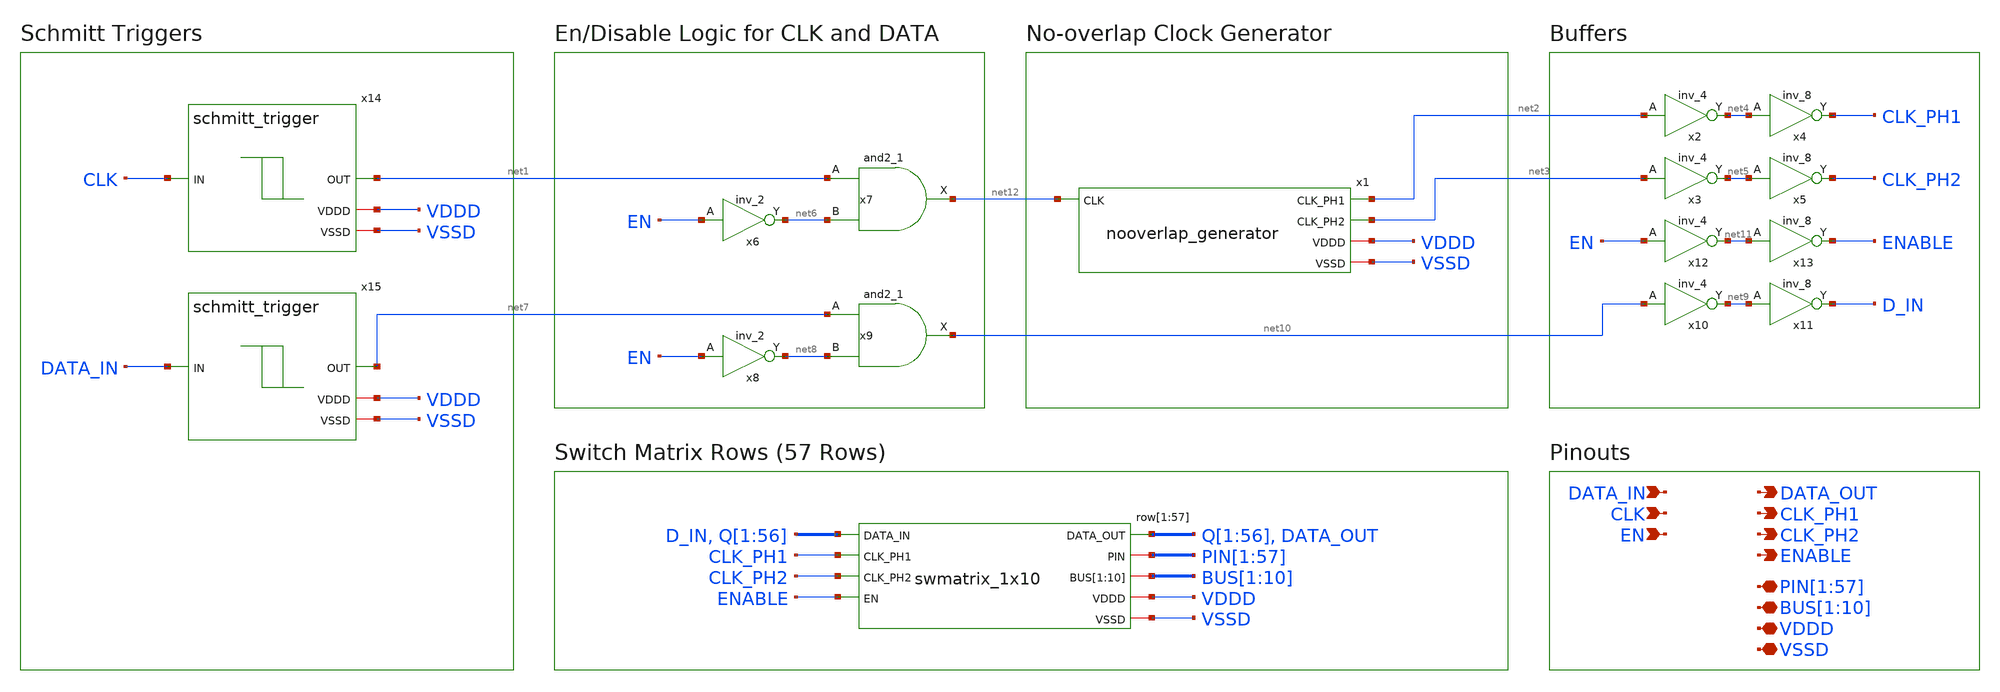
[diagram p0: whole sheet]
** sch_path: designs/libs/core_switch_matrix/swmatrix_57x10/swmatrix_57x10.sch
**.subckt swmatrix_57x10 DATA_IN CLK DATA_OUT VDDD VSSD EN
*+ PIN[1],PIN[2],PIN[3],PIN[4],PIN[5],PIN[6],PIN[7],PIN[8],PIN[9],PIN[10],PIN[11],PIN[12],PIN[13],PIN[14],PIN[15],PIN[16],PIN[17],PIN[18],PIN[19],PIN[20],PIN[21],PIN[22],PIN[23],PIN[24],PIN[25],PIN[26],PIN[27],PIN[28],PIN[29],PIN[30],PIN[31],PIN[32],PIN[33],PIN[34],PIN[35],PIN[36],PIN[37],PIN[38],PIN[39],PIN[40],PIN[41],PIN[42],PIN[43],PIN[44],PIN[45],PIN[46],PIN[47],PIN[48],PIN[49],PIN[50],PIN[51],PIN[52],PIN[53],PIN[54],PIN[55],PIN[56],PIN[57] BUS[1],BUS[2],BUS[3],BUS[4],BUS[5],BUS[6],BUS[7],BUS[8],BUS[9],BUS[10] CLK_PH1 CLK_PH2 ENABLE
*.ipin DATA_IN
*.ipin CLK
*.opin DATA_OUT
*.iopin VDDD
*.iopin VSSD
*.ipin EN
*.iopin
*+ PIN[1],PIN[2],PIN[3],PIN[4],PIN[5],PIN[6],PIN[7],PIN[8],PIN[9],PIN[10],PIN[11],PIN[12],PIN[13],PIN[14],PIN[15],PIN[16],PIN[17],PIN[18],PIN[19],PIN[20],PIN[21],PIN[22],PIN[23],PIN[24],PIN[25],PIN[26],PIN[27],PIN[28],PIN[29],PIN[30],PIN[31],PIN[32],PIN[33],PIN[34],PIN[35],PIN[36],PIN[37],PIN[38],PIN[39],PIN[40],PIN[41],PIN[42],PIN[43],PIN[44],PIN[45],PIN[46],PIN[47],PIN[48],PIN[49],PIN[50],PIN[51],PIN[52],PIN[53],PIN[54],PIN[55],PIN[56],PIN[57]
*.iopin BUS[1],BUS[2],BUS[3],BUS[4],BUS[5],BUS[6],BUS[7],BUS[8],BUS[9],BUS[10]
*.opin CLK_PH1
*.opin CLK_PH2
*.opin ENABLE
row[1] D_IN CLK_PH1 CLK_PH2 ENABLE Q[1] PIN[1] BUS[1] BUS[2] BUS[3] BUS[4] BUS[5] BUS[6] BUS[7]
+ BUS[8] BUS[9] BUS[10] VDDD VSSD swmatrix_1x10
row[2] Q[1] CLK_PH1 CLK_PH2 ENABLE Q[2] PIN[2] BUS[1] BUS[2] BUS[3] BUS[4] BUS[5] BUS[6] BUS[7]
+ BUS[8] BUS[9] BUS[10] VDDD VSSD swmatrix_1x10
row[3] Q[2] CLK_PH1 CLK_PH2 ENABLE Q[3] PIN[3] BUS[1] BUS[2] BUS[3] BUS[4] BUS[5] BUS[6] BUS[7]
+ BUS[8] BUS[9] BUS[10] VDDD VSSD swmatrix_1x10
row[4] Q[3] CLK_PH1 CLK_PH2 ENABLE Q[4] PIN[4] BUS[1] BUS[2] BUS[3] BUS[4] BUS[5] BUS[6] BUS[7]
+ BUS[8] BUS[9] BUS[10] VDDD VSSD swmatrix_1x10
row[5] Q[4] CLK_PH1 CLK_PH2 ENABLE Q[5] PIN[5] BUS[1] BUS[2] BUS[3] BUS[4] BUS[5] BUS[6] BUS[7]
+ BUS[8] BUS[9] BUS[10] VDDD VSSD swmatrix_1x10
row[6] Q[5] CLK_PH1 CLK_PH2 ENABLE Q[6] PIN[6] BUS[1] BUS[2] BUS[3] BUS[4] BUS[5] BUS[6] BUS[7]
+ BUS[8] BUS[9] BUS[10] VDDD VSSD swmatrix_1x10
row[7] Q[6] CLK_PH1 CLK_PH2 ENABLE Q[7] PIN[7] BUS[1] BUS[2] BUS[3] BUS[4] BUS[5] BUS[6] BUS[7]
+ BUS[8] BUS[9] BUS[10] VDDD VSSD swmatrix_1x10
row[8] Q[7] CLK_PH1 CLK_PH2 ENABLE Q[8] PIN[8] BUS[1] BUS[2] BUS[3] BUS[4] BUS[5] BUS[6] BUS[7]
+ BUS[8] BUS[9] BUS[10] VDDD VSSD swmatrix_1x10
row[9] Q[8] CLK_PH1 CLK_PH2 ENABLE Q[9] PIN[9] BUS[1] BUS[2] BUS[3] BUS[4] BUS[5] BUS[6] BUS[7]
+ BUS[8] BUS[9] BUS[10] VDDD VSSD swmatrix_1x10
row[10] Q[9] CLK_PH1 CLK_PH2 ENABLE Q[10] PIN[10] BUS[1] BUS[2] BUS[3] BUS[4] BUS[5] BUS[6] BUS[7]
+ BUS[8] BUS[9] BUS[10] VDDD VSSD swmatrix_1x10
row[11] Q[10] CLK_PH1 CLK_PH2 ENABLE Q[11] PIN[11] BUS[1] BUS[2] BUS[3] BUS[4] BUS[5] BUS[6] BUS[7]
+ BUS[8] BUS[9] BUS[10] VDDD VSSD swmatrix_1x10
row[12] Q[11] CLK_PH1 CLK_PH2 ENABLE Q[12] PIN[12] BUS[1] BUS[2] BUS[3] BUS[4] BUS[5] BUS[6] BUS[7]
+ BUS[8] BUS[9] BUS[10] VDDD VSSD swmatrix_1x10
row[13] Q[12] CLK_PH1 CLK_PH2 ENABLE Q[13] PIN[13] BUS[1] BUS[2] BUS[3] BUS[4] BUS[5] BUS[6] BUS[7]
+ BUS[8] BUS[9] BUS[10] VDDD VSSD swmatrix_1x10
row[14] Q[13] CLK_PH1 CLK_PH2 ENABLE Q[14] PIN[14] BUS[1] BUS[2] BUS[3] BUS[4] BUS[5] BUS[6] BUS[7]
+ BUS[8] BUS[9] BUS[10] VDDD VSSD swmatrix_1x10
row[15] Q[14] CLK_PH1 CLK_PH2 ENABLE Q[15] PIN[15] BUS[1] BUS[2] BUS[3] BUS[4] BUS[5] BUS[6] BUS[7]
+ BUS[8] BUS[9] BUS[10] VDDD VSSD swmatrix_1x10
row[16] Q[15] CLK_PH1 CLK_PH2 ENABLE Q[16] PIN[16] BUS[1] BUS[2] BUS[3] BUS[4] BUS[5] BUS[6] BUS[7]
+ BUS[8] BUS[9] BUS[10] VDDD VSSD swmatrix_1x10
row[17] Q[16] CLK_PH1 CLK_PH2 ENABLE Q[17] PIN[17] BUS[1] BUS[2] BUS[3] BUS[4] BUS[5] BUS[6] BUS[7]
+ BUS[8] BUS[9] BUS[10] VDDD VSSD swmatrix_1x10
row[18] Q[17] CLK_PH1 CLK_PH2 ENABLE Q[18] PIN[18] BUS[1] BUS[2] BUS[3] BUS[4] BUS[5] BUS[6] BUS[7]
+ BUS[8] BUS[9] BUS[10] VDDD VSSD swmatrix_1x10
row[19] Q[18] CLK_PH1 CLK_PH2 ENABLE Q[19] PIN[19] BUS[1] BUS[2] BUS[3] BUS[4] BUS[5] BUS[6] BUS[7]
+ BUS[8] BUS[9] BUS[10] VDDD VSSD swmatrix_1x10
row[20] Q[19] CLK_PH1 CLK_PH2 ENABLE Q[20] PIN[20] BUS[1] BUS[2] BUS[3] BUS[4] BUS[5] BUS[6] BUS[7]
+ BUS[8] BUS[9] BUS[10] VDDD VSSD swmatrix_1x10
row[21] Q[20] CLK_PH1 CLK_PH2 ENABLE Q[21] PIN[21] BUS[1] BUS[2] BUS[3] BUS[4] BUS[5] BUS[6] BUS[7]
+ BUS[8] BUS[9] BUS[10] VDDD VSSD swmatrix_1x10
row[22] Q[21] CLK_PH1 CLK_PH2 ENABLE Q[22] PIN[22] BUS[1] BUS[2] BUS[3] BUS[4] BUS[5] BUS[6] BUS[7]
+ BUS[8] BUS[9] BUS[10] VDDD VSSD swmatrix_1x10
row[23] Q[22] CLK_PH1 CLK_PH2 ENABLE Q[23] PIN[23] BUS[1] BUS[2] BUS[3] BUS[4] BUS[5] BUS[6] BUS[7]
+ BUS[8] BUS[9] BUS[10] VDDD VSSD swmatrix_1x10
row[24] Q[23] CLK_PH1 CLK_PH2 ENABLE Q[24] PIN[24] BUS[1] BUS[2] BUS[3] BUS[4] BUS[5] BUS[6] BUS[7]
+ BUS[8] BUS[9] BUS[10] VDDD VSSD swmatrix_1x10
row[25] Q[24] CLK_PH1 CLK_PH2 ENABLE Q[25] PIN[25] BUS[1] BUS[2] BUS[3] BUS[4] BUS[5] BUS[6] BUS[7]
+ BUS[8] BUS[9] BUS[10] VDDD VSSD swmatrix_1x10
row[26] Q[25] CLK_PH1 CLK_PH2 ENABLE Q[26] PIN[26] BUS[1] BUS[2] BUS[3] BUS[4] BUS[5] BUS[6] BUS[7]
+ BUS[8] BUS[9] BUS[10] VDDD VSSD swmatrix_1x10
row[27] Q[26] CLK_PH1 CLK_PH2 ENABLE Q[27] PIN[27] BUS[1] BUS[2] BUS[3] BUS[4] BUS[5] BUS[6] BUS[7]
+ BUS[8] BUS[9] BUS[10] VDDD VSSD swmatrix_1x10
row[28] Q[27] CLK_PH1 CLK_PH2 ENABLE Q[28] PIN[28] BUS[1] BUS[2] BUS[3] BUS[4] BUS[5] BUS[6] BUS[7]
+ BUS[8] BUS[9] BUS[10] VDDD VSSD swmatrix_1x10
row[29] Q[28] CLK_PH1 CLK_PH2 ENABLE Q[29] PIN[29] BUS[1] BUS[2] BUS[3] BUS[4] BUS[5] BUS[6] BUS[7]
+ BUS[8] BUS[9] BUS[10] VDDD VSSD swmatrix_1x10
row[30] Q[29] CLK_PH1 CLK_PH2 ENABLE Q[30] PIN[30] BUS[1] BUS[2] BUS[3] BUS[4] BUS[5] BUS[6] BUS[7]
+ BUS[8] BUS[9] BUS[10] VDDD VSSD swmatrix_1x10
row[31] Q[30] CLK_PH1 CLK_PH2 ENABLE Q[31] PIN[31] BUS[1] BUS[2] BUS[3] BUS[4] BUS[5] BUS[6] BUS[7]
+ BUS[8] BUS[9] BUS[10] VDDD VSSD swmatrix_1x10
row[32] Q[31] CLK_PH1 CLK_PH2 ENABLE Q[32] PIN[32] BUS[1] BUS[2] BUS[3] BUS[4] BUS[5] BUS[6] BUS[7]
+ BUS[8] BUS[9] BUS[10] VDDD VSSD swmatrix_1x10
row[33] Q[32] CLK_PH1 CLK_PH2 ENABLE Q[33] PIN[33] BUS[1] BUS[2] BUS[3] BUS[4] BUS[5] BUS[6] BUS[7]
+ BUS[8] BUS[9] BUS[10] VDDD VSSD swmatrix_1x10
row[34] Q[33] CLK_PH1 CLK_PH2 ENABLE Q[34] PIN[34] BUS[1] BUS[2] BUS[3] BUS[4] BUS[5] BUS[6] BUS[7]
+ BUS[8] BUS[9] BUS[10] VDDD VSSD swmatrix_1x10
row[35] Q[34] CLK_PH1 CLK_PH2 ENABLE Q[35] PIN[35] BUS[1] BUS[2] BUS[3] BUS[4] BUS[5] BUS[6] BUS[7]
+ BUS[8] BUS[9] BUS[10] VDDD VSSD swmatrix_1x10
row[36] Q[35] CLK_PH1 CLK_PH2 ENABLE Q[36] PIN[36] BUS[1] BUS[2] BUS[3] BUS[4] BUS[5] BUS[6] BUS[7]
+ BUS[8] BUS[9] BUS[10] VDDD VSSD swmatrix_1x10
row[37] Q[36] CLK_PH1 CLK_PH2 ENABLE Q[37] PIN[37] BUS[1] BUS[2] BUS[3] BUS[4] BUS[5] BUS[6] BUS[7]
+ BUS[8] BUS[9] BUS[10] VDDD VSSD swmatrix_1x10
row[38] Q[37] CLK_PH1 CLK_PH2 ENABLE Q[38] PIN[38] BUS[1] BUS[2] BUS[3] BUS[4] BUS[5] BUS[6] BUS[7]
+ BUS[8] BUS[9] BUS[10] VDDD VSSD swmatrix_1x10
row[39] Q[38] CLK_PH1 CLK_PH2 ENABLE Q[39] PIN[39] BUS[1] BUS[2] BUS[3] BUS[4] BUS[5] BUS[6] BUS[7]
+ BUS[8] BUS[9] BUS[10] VDDD VSSD swmatrix_1x10
row[40] Q[39] CLK_PH1 CLK_PH2 ENABLE Q[40] PIN[40] BUS[1] BUS[2] BUS[3] BUS[4] BUS[5] BUS[6] BUS[7]
+ BUS[8] BUS[9] BUS[10] VDDD VSSD swmatrix_1x10
row[41] Q[40] CLK_PH1 CLK_PH2 ENABLE Q[41] PIN[41] BUS[1] BUS[2] BUS[3] BUS[4] BUS[5] BUS[6] BUS[7]
+ BUS[8] BUS[9] BUS[10] VDDD VSSD swmatrix_1x10
row[42] Q[41] CLK_PH1 CLK_PH2 ENABLE Q[42] PIN[42] BUS[1] BUS[2] BUS[3] BUS[4] BUS[5] BUS[6] BUS[7]
+ BUS[8] BUS[9] BUS[10] VDDD VSSD swmatrix_1x10
row[43] Q[42] CLK_PH1 CLK_PH2 ENABLE Q[43] PIN[43] BUS[1] BUS[2] BUS[3] BUS[4] BUS[5] BUS[6] BUS[7]
+ BUS[8] BUS[9] BUS[10] VDDD VSSD swmatrix_1x10
row[44] Q[43] CLK_PH1 CLK_PH2 ENABLE Q[44] PIN[44] BUS[1] BUS[2] BUS[3] BUS[4] BUS[5] BUS[6] BUS[7]
+ BUS[8] BUS[9] BUS[10] VDDD VSSD swmatrix_1x10
row[45] Q[44] CLK_PH1 CLK_PH2 ENABLE Q[45] PIN[45] BUS[1] BUS[2] BUS[3] BUS[4] BUS[5] BUS[6] BUS[7]
+ BUS[8] BUS[9] BUS[10] VDDD VSSD swmatrix_1x10
row[46] Q[45] CLK_PH1 CLK_PH2 ENABLE Q[46] PIN[46] BUS[1] BUS[2] BUS[3] BUS[4] BUS[5] BUS[6] BUS[7]
+ BUS[8] BUS[9] BUS[10] VDDD VSSD swmatrix_1x10
row[47] Q[46] CLK_PH1 CLK_PH2 ENABLE Q[47] PIN[47] BUS[1] BUS[2] BUS[3] BUS[4] BUS[5] BUS[6] BUS[7]
+ BUS[8] BUS[9] BUS[10] VDDD VSSD swmatrix_1x10
row[48] Q[47] CLK_PH1 CLK_PH2 ENABLE Q[48] PIN[48] BUS[1] BUS[2] BUS[3] BUS[4] BUS[5] BUS[6] BUS[7]
+ BUS[8] BUS[9] BUS[10] VDDD VSSD swmatrix_1x10
row[49] Q[48] CLK_PH1 CLK_PH2 ENABLE Q[49] PIN[49] BUS[1] BUS[2] BUS[3] BUS[4] BUS[5] BUS[6] BUS[7]
+ BUS[8] BUS[9] BUS[10] VDDD VSSD swmatrix_1x10
row[50] Q[49] CLK_PH1 CLK_PH2 ENABLE Q[50] PIN[50] BUS[1] BUS[2] BUS[3] BUS[4] BUS[5] BUS[6] BUS[7]
+ BUS[8] BUS[9] BUS[10] VDDD VSSD swmatrix_1x10
row[51] Q[50] CLK_PH1 CLK_PH2 ENABLE Q[51] PIN[51] BUS[1] BUS[2] BUS[3] BUS[4] BUS[5] BUS[6] BUS[7]
+ BUS[8] BUS[9] BUS[10] VDDD VSSD swmatrix_1x10
row[52] Q[51] CLK_PH1 CLK_PH2 ENABLE Q[52] PIN[52] BUS[1] BUS[2] BUS[3] BUS[4] BUS[5] BUS[6] BUS[7]
+ BUS[8] BUS[9] BUS[10] VDDD VSSD swmatrix_1x10
row[53] Q[52] CLK_PH1 CLK_PH2 ENABLE Q[53] PIN[53] BUS[1] BUS[2] BUS[3] BUS[4] BUS[5] BUS[6] BUS[7]
+ BUS[8] BUS[9] BUS[10] VDDD VSSD swmatrix_1x10
row[54] Q[53] CLK_PH1 CLK_PH2 ENABLE Q[54] PIN[54] BUS[1] BUS[2] BUS[3] BUS[4] BUS[5] BUS[6] BUS[7]
+ BUS[8] BUS[9] BUS[10] VDDD VSSD swmatrix_1x10
row[55] Q[54] CLK_PH1 CLK_PH2 ENABLE Q[55] PIN[55] BUS[1] BUS[2] BUS[3] BUS[4] BUS[5] BUS[6] BUS[7]
+ BUS[8] BUS[9] BUS[10] VDDD VSSD swmatrix_1x10
row[56] Q[55] CLK_PH1 CLK_PH2 ENABLE Q[56] PIN[56] BUS[1] BUS[2] BUS[3] BUS[4] BUS[5] BUS[6] BUS[7]
+ BUS[8] BUS[9] BUS[10] VDDD VSSD swmatrix_1x10
row[57] Q[56] CLK_PH1 CLK_PH2 ENABLE DATA_OUT PIN[57] BUS[1] BUS[2] BUS[3] BUS[4] BUS[5] BUS[6]
+ BUS[7] BUS[8] BUS[9] BUS[10] VDDD VSSD swmatrix_1x10
x1 net12 net2 net3 VDDD VSSD nooverlap_generator
x2 net2 VSSD VDDD VSSD VDDD net4 gf180mcu_fd_sc_mcu9t5v0__inv_4
x3 net3 VSSD VDDD VSSD VDDD net5 gf180mcu_fd_sc_mcu9t5v0__inv_4
x4 net4 VSSD VDDD VSSD VDDD CLK_PH1 gf180mcu_fd_sc_mcu9t5v0__inv_8
x5 net5 VSSD VDDD VSSD VDDD CLK_PH2 gf180mcu_fd_sc_mcu9t5v0__inv_8
x6 EN VSSD VDDD VSSD VDDD net6 gf180mcu_fd_sc_mcu9t5v0__inv_2
x7 net1 net6 VSSD VDDD VSSD VDDD net12 gf180mcu_fd_sc_mcu9t5v0__and2_1
x8 EN VSSD VDDD VSSD VDDD net8 gf180mcu_fd_sc_mcu9t5v0__inv_2
x9 net7 net8 VSSD VDDD VSSD VDDD net10 gf180mcu_fd_sc_mcu9t5v0__and2_1
x10 net10 VSSD VDDD VSSD VDDD net9 gf180mcu_fd_sc_mcu9t5v0__inv_4
x11 net9 VSSD VDDD VSSD VDDD D_IN gf180mcu_fd_sc_mcu9t5v0__inv_8
x12 EN VSSD VDDD VSSD VDDD net11 gf180mcu_fd_sc_mcu9t5v0__inv_4
x13 net11 VSSD VDDD VSSD VDDD ENABLE gf180mcu_fd_sc_mcu9t5v0__inv_8
x14 CLK net1 VDDD VSSD schmitt_trigger
x15 DATA_IN net7 VDDD VSSD schmitt_trigger
**.ends

* expanding   symbol:  libs/core_switch_matrix/swmatrix_1x10/swmatrix_1x10.sym # of pins=9
** sym_path: designs/libs/core_switch_matrix/swmatrix_1x10/swmatrix_1x10.sym
** sch_path: designs/libs/core_switch_matrix/swmatrix_1x10/swmatrix_1x10.sch
.subckt swmatrix_1x10 DATA_IN CLK_PH1 CLK_PH2 EN DATA_OUT PIN BUS[1] BUS[2] BUS[3] BUS[4] BUS[5]
+ BUS[6] BUS[7] BUS[8] BUS[9] BUS[10] VDDD VSSD
*.ipin DATA_IN
*.ipin CLK_PH1
*.ipin CLK_PH2
*.opin DATA_OUT
*.iopin VDDD
*.iopin VSSD
*.ipin EN
*.iopin PIN
*.iopin BUS[1],BUS[2],BUS[3],BUS[4],BUS[5],BUS[6],BUS[7],BUS[8],BUS[9],BUS[10]
xsw[1] DATA_IN CLK_PH1 CLK_PH2 EN Q[1] PIN BUS[1] VDDD VSSD switch_cell
xsw[2] Q[1] CLK_PH1 CLK_PH2 EN Q[2] PIN BUS[2] VDDD VSSD switch_cell
xsw[3] Q[2] CLK_PH1 CLK_PH2 EN Q[3] PIN BUS[3] VDDD VSSD switch_cell
xsw[4] Q[3] CLK_PH1 CLK_PH2 EN Q[4] PIN BUS[4] VDDD VSSD switch_cell
xsw[5] Q[4] CLK_PH1 CLK_PH2 EN Q[5] PIN BUS[5] VDDD VSSD switch_cell
xsw[6] Q[5] CLK_PH1 CLK_PH2 EN Q[6] PIN BUS[6] VDDD VSSD switch_cell
xsw[7] Q[6] CLK_PH1 CLK_PH2 EN Q[7] PIN BUS[7] VDDD VSSD switch_cell
xsw[8] Q[7] CLK_PH1 CLK_PH2 EN Q[8] PIN BUS[8] VDDD VSSD switch_cell
xsw[9] Q[8] CLK_PH1 CLK_PH2 EN Q[9] PIN BUS[9] VDDD VSSD switch_cell
xsw[10] Q[9] CLK_PH1 CLK_PH2 EN DATA_OUT PIN BUS[10] VDDD VSSD switch_cell
.ends


* expanding   symbol:  libs/core_switch_matrix/nooverlap_generator/nooverlap_generator.sym # of
*+ pins=5
** sym_path: designs/libs/core_switch_matrix/nooverlap_generator/nooverlap_generator.sym
** sch_path: designs/libs/core_switch_matrix/nooverlap_generator/nooverlap_generator.sch
.subckt nooverlap_generator CLK CLK_PH1 CLK_PH2 VDDD VSSD
*.ipin CLK
*.opin CLK_PH1
*.iopin VDDD
*.iopin VSSD
*.opin CLK_PH2
x1 net17 net15 VSSD VDDD VSSD VDDD net1 gf180mcu_fd_sc_mcu9t5v0__nand2_1
x2 net16 net18 VSSD VDDD VSSD VDDD net8 gf180mcu_fd_sc_mcu9t5v0__nand2_1
x3 net1 VSSD VDDD VSSD VDDD CLK_PH2 gf180mcu_fd_sc_mcu9t5v0__inv_1
x4 CLK_PH2 VSSD VDDD VSSD VDDD net2 gf180mcu_fd_sc_mcu9t5v0__inv_1
x5 net2 VSSD VDDD VSSD VDDD net3 gf180mcu_fd_sc_mcu9t5v0__inv_1
x6 net3 VSSD VDDD VSSD VDDD net4 gf180mcu_fd_sc_mcu9t5v0__inv_1
x7 net4 VSSD VDDD VSSD VDDD net5 gf180mcu_fd_sc_mcu9t5v0__inv_1
x8 net5 VSSD VDDD VSSD VDDD net6 gf180mcu_fd_sc_mcu9t5v0__inv_1
x9 net6 VSSD VDDD VSSD VDDD net7 gf180mcu_fd_sc_mcu9t5v0__inv_1
x10 net7 VSSD VDDD VSSD VDDD net16 gf180mcu_fd_sc_mcu9t5v0__inv_1
x11 net8 VSSD VDDD VSSD VDDD CLK_PH1 gf180mcu_fd_sc_mcu9t5v0__inv_1
x12 CLK_PH1 VSSD VDDD VSSD VDDD net9 gf180mcu_fd_sc_mcu9t5v0__inv_1
x13 net9 VSSD VDDD VSSD VDDD net10 gf180mcu_fd_sc_mcu9t5v0__inv_1
x14 net10 VSSD VDDD VSSD VDDD net11 gf180mcu_fd_sc_mcu9t5v0__inv_1
x15 net11 VSSD VDDD VSSD VDDD net12 gf180mcu_fd_sc_mcu9t5v0__inv_1
x16 net12 VSSD VDDD VSSD VDDD net13 gf180mcu_fd_sc_mcu9t5v0__inv_1
x17 net13 VSSD VDDD VSSD VDDD net14 gf180mcu_fd_sc_mcu9t5v0__inv_1
x18 net14 VSSD VDDD VSSD VDDD net15 gf180mcu_fd_sc_mcu9t5v0__inv_1
x19 net17 VSSD VDDD VSSD VDDD net18 gf180mcu_fd_sc_mcu9t5v0__inv_1
x20 CLK VSSD VDDD VSSD VDDD net17 gf180mcu_fd_sc_mcu9t5v0__inv_1
.ends


* expanding   symbol:  libs/core_switch_matrix/schmitt_trigger/schmitt_trigger.sym # of pins=4
** sym_path: designs/libs/core_switch_matrix/schmitt_trigger/schmitt_trigger.sym
** sch_path: designs/libs/core_switch_matrix/schmitt_trigger/schmitt_trigger.sch
.subckt schmitt_trigger IN OUT VDDD VSSD
*.ipin IN
*.opin OUT
*.iopin VDDD
*.iopin VSSD
XM1 net1 IN VSSD VSSD nfet_03v3 L=0.28u W=0.5u nf=1 ad='int((nf+1)/2) * W/nf * 0.18u' as='int((nf+2)/2) * W/nf * 0.18u'
+ pd='2*int((nf+1)/2) * (W/nf + 0.18u)' ps='2*int((nf+2)/2) * (W/nf + 0.18u)' nrd='0.18u / W' nrs='0.18u / W'
+ sa=0 sb=0 sd=0 m=12
XM2 net2 IN net1 VSSD nfet_03v3 L=0.28u W=0.5u nf=1 ad='int((nf+1)/2) * W/nf * 0.18u' as='int((nf+2)/2) * W/nf * 0.18u'
+ pd='2*int((nf+1)/2) * (W/nf + 0.18u)' ps='2*int((nf+2)/2) * (W/nf + 0.18u)' nrd='0.18u / W' nrs='0.18u / W'
+ sa=0 sb=0 sd=0 m=12
XM3 VDDD net2 net1 VSSD nfet_03v3 L=0.56u W=0.5u nf=1 ad='int((nf+1)/2) * W/nf * 0.18u' as='int((nf+2)/2) * W/nf * 0.18u'
+ pd='2*int((nf+1)/2) * (W/nf + 0.18u)' ps='2*int((nf+2)/2) * (W/nf + 0.18u)' nrd='0.18u / W' nrs='0.18u / W'
+ sa=0 sb=0 sd=0 m=1
XM4 net3 IN VDDD VDDD pfet_03v3 L=0.28u W=1.5u nf=1 ad='int((nf+1)/2) * W/nf * 0.18u' as='int((nf+2)/2) * W/nf * 0.18u'
+ pd='2*int((nf+1)/2) * (W/nf + 0.18u)' ps='2*int((nf+2)/2) * (W/nf + 0.18u)' nrd='0.18u / W' nrs='0.18u / W'
+ sa=0 sb=0 sd=0 m=12
XM5 net2 IN net3 VDDD pfet_03v3 L=0.28u W=1.5u nf=1 ad='int((nf+1)/2) * W/nf * 0.18u' as='int((nf+2)/2) * W/nf * 0.18u'
+ pd='2*int((nf+1)/2) * (W/nf + 0.18u)' ps='2*int((nf+2)/2) * (W/nf + 0.18u)' nrd='0.18u / W' nrs='0.18u / W'
+ sa=0 sb=0 sd=0 m=12
XM6 VSSD net2 net3 VDDD pfet_03v3 L=0.56u W=1.5u nf=1 ad='int((nf+1)/2) * W/nf * 0.18u' as='int((nf+2)/2) * W/nf * 0.18u'
+ pd='2*int((nf+1)/2) * (W/nf + 0.18u)' ps='2*int((nf+2)/2) * (W/nf + 0.18u)' nrd='0.18u / W' nrs='0.18u / W'
+ sa=0 sb=0 sd=0 m=1
XM7 OUT net2 VSSD VSSD nfet_03v3 L=0.28u W=0.5u nf=1 ad='int((nf+1)/2) * W/nf * 0.18u' as='int((nf+2)/2) * W/nf * 0.18u'
+ pd='2*int((nf+1)/2) * (W/nf + 0.18u)' ps='2*int((nf+2)/2) * (W/nf + 0.18u)' nrd='0.18u / W' nrs='0.18u / W'
+ sa=0 sb=0 sd=0 m=2
XM8 OUT net2 VDDD VDDD pfet_03v3 L=0.28u W=1.5u nf=1 ad='int((nf+1)/2) * W/nf * 0.18u' as='int((nf+2)/2) * W/nf * 0.18u'
+ pd='2*int((nf+1)/2) * (W/nf + 0.18u)' ps='2*int((nf+2)/2) * (W/nf + 0.18u)' nrd='0.18u / W' nrs='0.18u / W'
+ sa=0 sb=0 sd=0 m=2
.ends


* expanding   symbol:  libs/core_switch_matrix/switch_cell/switch_cell.sym # of pins=9
** sym_path: designs/libs/core_switch_matrix/switch_cell/switch_cell.sym
** sch_path: designs/libs/core_switch_matrix/switch_cell/switch_cell.sch
.subckt switch_cell DATA_IN CLK_PH1 CLK_PH2 EN DATA_OUT T1 T2 VDDD VSSD
*.ipin DATA_IN
*.ipin CLK_PH1
*.ipin CLK_PH2
*.opin DATA_OUT
*.iopin VDDD
*.iopin VSSD
*.ipin EN
*.iopin T1
*.iopin T2
x1 DATA_IN CLK_PH1 CLK_PH2 DATA_OUT VDDD VSSD dff_2ph_clk
x2 DATA_OUT EN VDDD VSSD T1 T2 tgate
.ends


* expanding   symbol:  libs/core_switch_matrix/dff_2ph_clk/dff_2ph_clk.sym # of pins=6
** sym_path: designs/libs/core_switch_matrix/dff_2ph_clk/dff_2ph_clk.sym
** sch_path: designs/libs/core_switch_matrix/dff_2ph_clk/dff_2ph_clk.sch
.subckt dff_2ph_clk D CLK_PH1 CLK_PH2 Q VDDD VSSD
*.ipin D
*.ipin CLK_PH1
*.ipin CLK_PH2
*.opin Q
*.iopin VDDD
*.iopin VSSD
x1 D CLK_PH1 net1 VDDD VDDD VSSD VSSD gf180mcu_fd_sc_mcu9t5v0__latq_1
x2 net1 CLK_PH2 Q VDDD VDDD VSSD VSSD gf180mcu_fd_sc_mcu9t5v0__latq_1
**** begin user architecture code

.include /foss/pdks/gf180mcuD/libs.ref/gf180mcu_fd_sc_mcu9t5v0/spice/gf180mcu_fd_sc_mcu9t5v0.spice

**** end user architecture code
.ends


* expanding   symbol:  libs/core_switch_matrix/tgate/tgate.sym # of pins=6
** sym_path: designs/libs/core_switch_matrix/tgate/tgate.sym
** sch_path: designs/libs/core_switch_matrix/tgate/tgate.sch
.subckt tgate CON EN VDDD VSSD T1 T2
*.ipin CON
*.ipin EN
*.iopin VDDD
*.iopin VSSD
*.iopin T1
*.iopin T2
XM1 T2 NCON T1 VSSD nfet_03v3 L=0.28u W=4u nf=1 ad='int((nf+1)/2) * W/nf * 0.18u' as='int((nf+2)/2) * W/nf * 0.18u'
+ pd='2*int((nf+1)/2) * (W/nf + 0.18u)' ps='2*int((nf+2)/2) * (W/nf + 0.18u)' nrd='0.18u / W' nrs='0.18u / W'
+ sa=0 sb=0 sd=0 m=6
XM2 T2 PCON T1 VDDD pfet_03v3 L=0.28u W=4u nf=1 ad='int((nf+1)/2) * W/nf * 0.18u' as='int((nf+2)/2) * W/nf * 0.18u'
+ pd='2*int((nf+1)/2) * (W/nf + 0.18u)' ps='2*int((nf+2)/2) * (W/nf + 0.18u)' nrd='0.18u / W' nrs='0.18u / W'
+ sa=0 sb=0 sd=0 m=18
x1 CON EN VSSD VDDD VSSD VDDD net1 gf180mcu_fd_sc_mcu9t5v0__nand2_1
x2 net1 VSSD VDDD VSSD VDDD NCON gf180mcu_fd_sc_mcu9t5v0__inv_1
x3 NCON VSSD VDDD VSSD VDDD PCON gf180mcu_fd_sc_mcu9t5v0__inv_1
**** begin user architecture code

.include /foss/pdks/gf180mcuD/libs.ref/gf180mcu_fd_sc_mcu9t5v0/spice/gf180mcu_fd_sc_mcu9t5v0.spice

**** end user architecture code
.ends

.end
